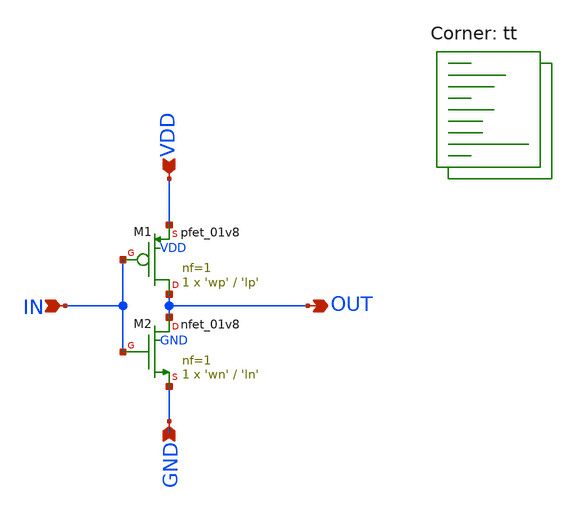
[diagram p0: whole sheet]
** sch_path: inverter.sch
**.subckt inverter IN VDD OUT GND
*.ipin IN
*.ipin VDD
*.opin OUT
*.ipin GND
XM2 OUT IN GND GND sky130_fd_pr__nfet_01v8 L='ln' W='wn' nf=1 ad='int((nf+1)/2) * W/nf * 0.29' as='int((nf+2)/2) * W/nf * 0.29'
+ pd='2*int((nf+1)/2) * (W/nf + 0.29)' ps='2*int((nf+2)/2) * (W/nf + 0.29)' nrd='0.29 / W' nrs='0.29 / W'
+ sa=0 sb=0 sd=0 mult=1 m=1
XM1 OUT IN VDD VDD sky130_fd_pr__pfet_01v8 L='lp' W='wp' nf=1 ad='int((nf+1)/2) * W/nf * 0.29' as='int((nf+2)/2) * W/nf * 0.29'
+ pd='2*int((nf+1)/2) * (W/nf + 0.29)' ps='2*int((nf+2)/2) * (W/nf + 0.29)' nrd='0.29 / W' nrs='0.29 / W'
+ sa=0 sb=0 sd=0 mult=1 m=1
**** begin user architecture code



.options savecurrents

.control
save all
dc vgs 0 1.8 0.01
let id_nmos=@m.xm3.msky130_fd_pr__nfet_01v8[id]
let id_pmos=@m.xm4.msky130_fd_pr__pfet_01v8[id]

*print @m.xm3.msky130_fd_pr__pfet_01v8[W]



*rise time, fall time

*plot deriv(sqrt(id_nmos))^2/deriv(sqrt(id_pmos))^2 title 'V_DD characteristic' xlabel 'V_DD' ylabel
*+ 'Ratio of derivatives'

*write characterization.raw

set appendwrite
.endc


.lib $::SKYWATER_MODELS/sky130.lib.spice tt
**** end user architecture code
**.ends
.end
